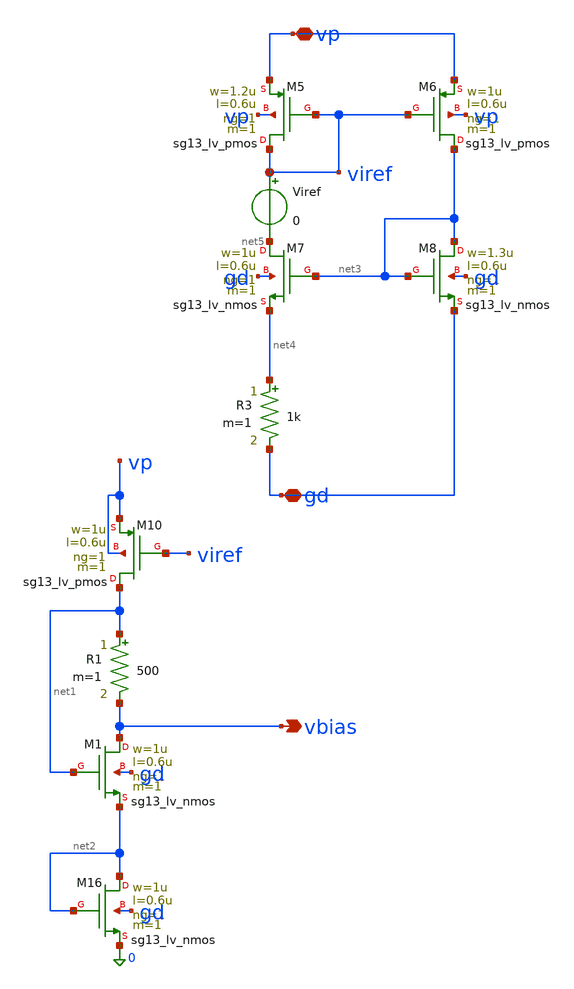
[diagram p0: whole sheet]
** sch_path: charge_pump/vbias.sch
**.subckt vbias vp gd vbias
*.iopin vp
*.iopin gd
*.opin vbias
XM16 net2 net2 0 gd sg13_lv_nmos w=1u l=0.6u ng=1 m=1 mm_ok=1
XM1 vbias net1 net2 gd sg13_lv_nmos w=1u l=0.6u ng=1 m=1 mm_ok=1
R1 net1 vbias 500 m=1
XM5 viref viref vp vp sg13_lv_pmos w=1.2u l=0.6u ng=1 m=1 mm_ok=1
XM6 net3 viref vp vp sg13_lv_pmos w=1u l=0.6u ng=1 m=1 mm_ok=1
XM7 net5 net3 net4 gd sg13_lv_nmos w=1u l=0.6u ng=1 m=1 mm_ok=1
XM8 net3 net3 gd gd sg13_lv_nmos w=1.3u l=0.6u ng=1 m=1 mm_ok=1
R3 net4 gd 1k m=1
XM10 net1 viref vp vp sg13_lv_pmos w=1u l=0.6u ng=1 m=1 mm_ok=1
Viref viref net5 0
**.ends
.end
